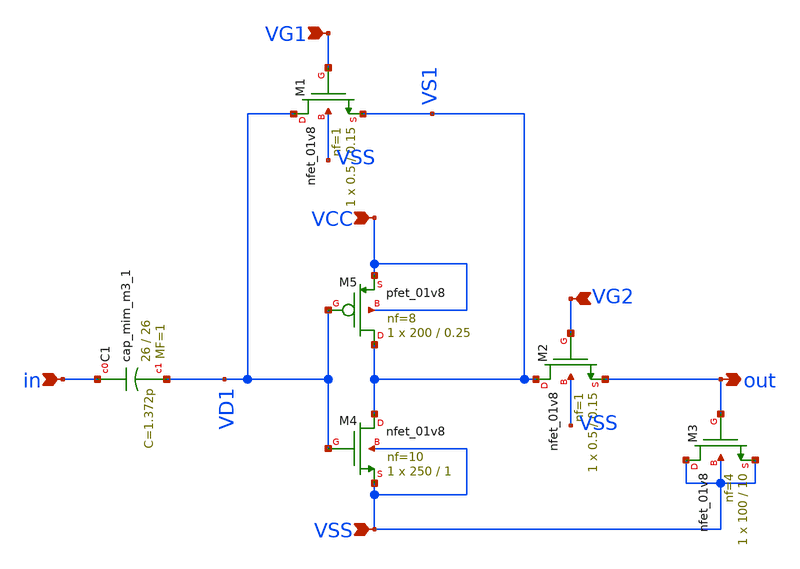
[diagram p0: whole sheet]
** sch_path: Amplifier_Inv/xschem/v4/inv_sky130_a_v4.sch
**.subckt inv_sky130_a_v4 in out VG1 VG2 VSS VCC
*.ipin in
*.opin out
*.ipin VG1
*.ipin VG2
*.ipin VSS
*.ipin VCC
XC1 in VD1 sky130_fd_pr__cap_mim_m3_1 W=26 L=26 MF=1 m=1
XM4 VS1 VD1 VSS VSS sky130_fd_pr__nfet_01v8 L=1 W=250 nf=10 ad='int((10 + 1)/2) * 250 / 10 * 0.29' as='int((10 + 2)/2) * 250 / 10 * 0.29'
+ pd='2*int((10 + 1)/2) * (250 / 10 + 0.29)' ps='2*int((10 + 2)/2) * (250 / 10 + 0.29)' nrd='0.29 / 250 '
+ nrs='0.29 / 250 ' sa=0 sb=0 sd=0 mult=1 m=1
XM5 VS1 VD1 VCC VCC sky130_fd_pr__pfet_01v8 L=0.25 W=200 nf=8 ad='int((nf+1)/2) * W/nf * 0.29' as='int((nf+2)/2) * W/nf * 0.29'
+ pd='2*int((nf+1)/2) * (W/nf + 0.29)' ps='2*int((nf+2)/2) * (W/nf + 0.29)' nrd='0.29 / W' nrs='0.29 / W'
+ sa=0 sb=0 sd=0 mult=1 m=1
XM2 VS1 VG2 out VSS sky130_fd_pr__nfet_01v8 L=0.15 W=0.5 nf=1 ad='int((1 + 1)/2) * 0.5 / 1 * 0.29' as='int((1 + 2)/2) * 0.5 / 1 * 0.29'
+ pd='2*int((1 + 1)/2) * (0.5 / 1 + 0.29)' ps='2*int((1 + 2)/2) * (0.5 / 1 + 0.29)' nrd='0.29 / 0.5 ' nrs='0.29 / 0.5 '
+ sa=0 sb=0 sd=0 mult=1 m=1
XM3 VSS out VSS VSS sky130_fd_pr__nfet_01v8 L=10 W=100 nf=4 ad='int((4 + 1)/2) * 100 / 4 * 0.29' as='int((4 + 2)/2) * 100 / 4 * 0.29'
+ pd='2*int((4 + 1)/2) * (100 / 4 + 0.29)' ps='2*int((4 + 2)/2) * (100 / 4 + 0.29)' nrd='0.29 / 100 ' nrs='0.29 / 100 '
+ sa=0 sb=0 sd=0 mult=1 m=1
XM1 VD1 VG1 VS1 VSS sky130_fd_pr__nfet_01v8 L=0.15 W=0.5 nf=1 ad='int((1 + 1)/2) * 0.5 / 1 * 0.29' as='int((1 + 2)/2) * 0.5 / 1 * 0.29'
+ pd='2*int((1 + 1)/2) * (0.5 / 1 + 0.29)' ps='2*int((1 + 2)/2) * (0.5 / 1 + 0.29)' nrd='0.29 / 0.5 ' nrs='0.29 / 0.5 '
+ sa=0 sb=0 sd=0 mult=1 m=1
**** begin user architecture code

** opencircuitdesign pdks install
.lib $::SKYWATER_MODELS/sky130.lib.spice tt


**** end user architecture code
**.ends
.end
